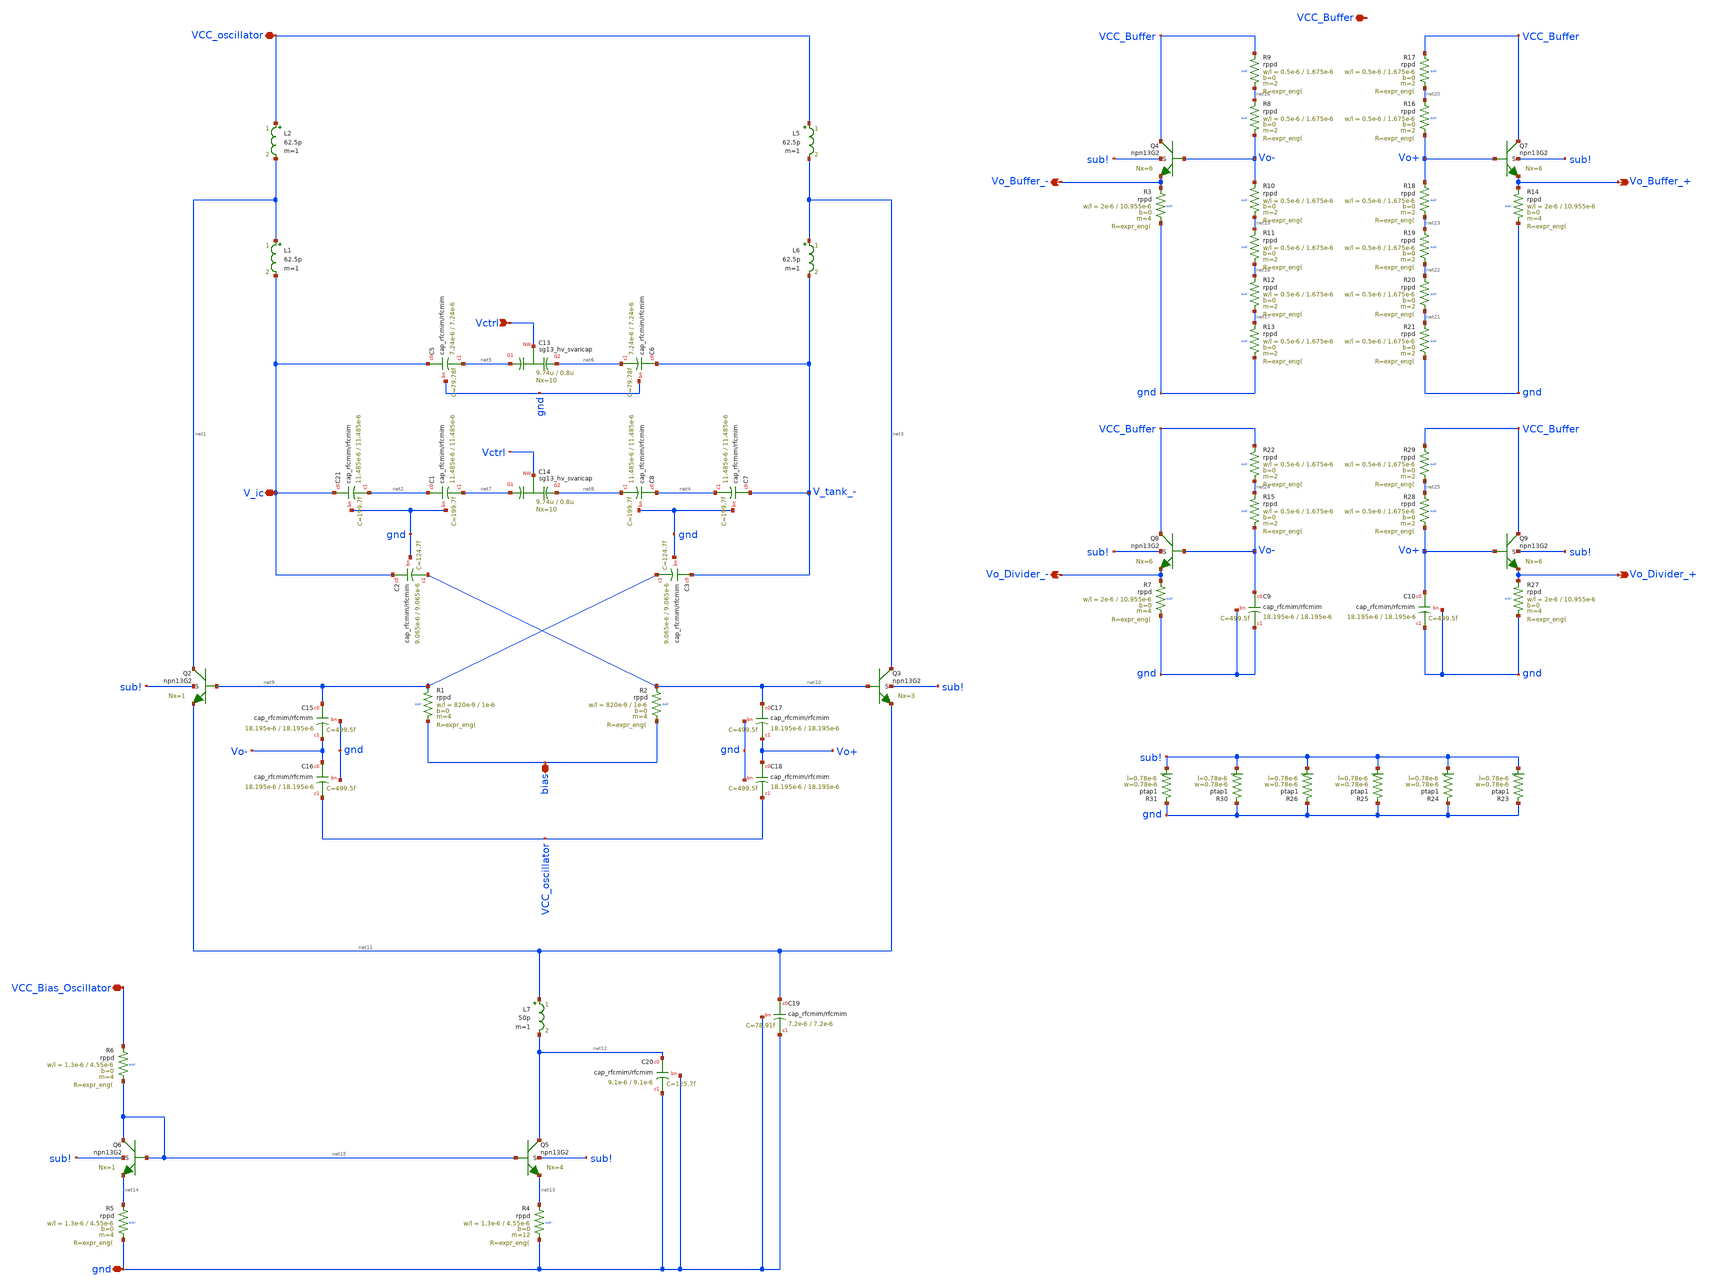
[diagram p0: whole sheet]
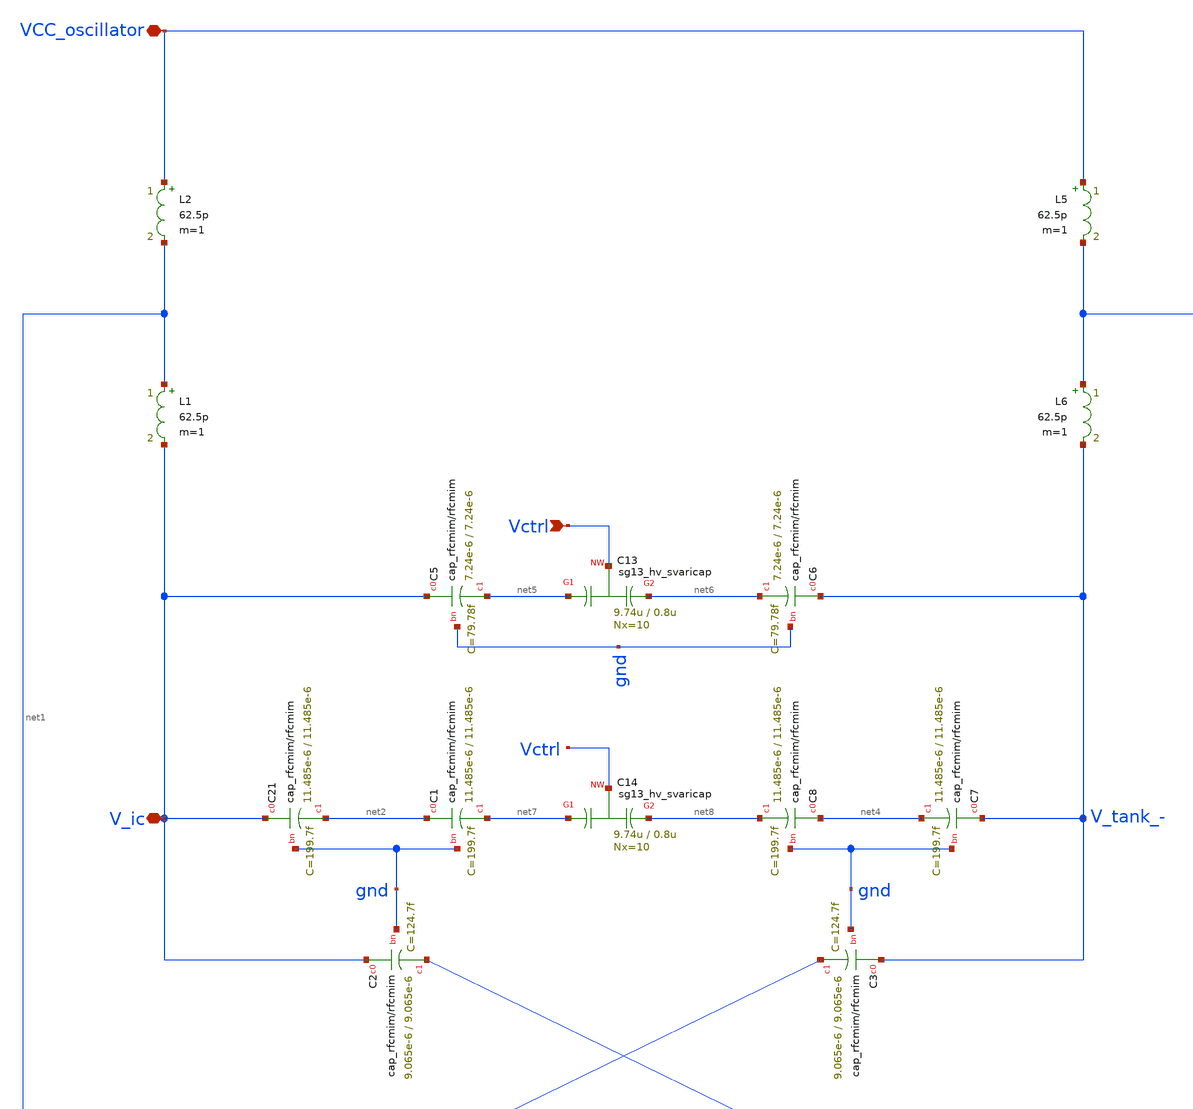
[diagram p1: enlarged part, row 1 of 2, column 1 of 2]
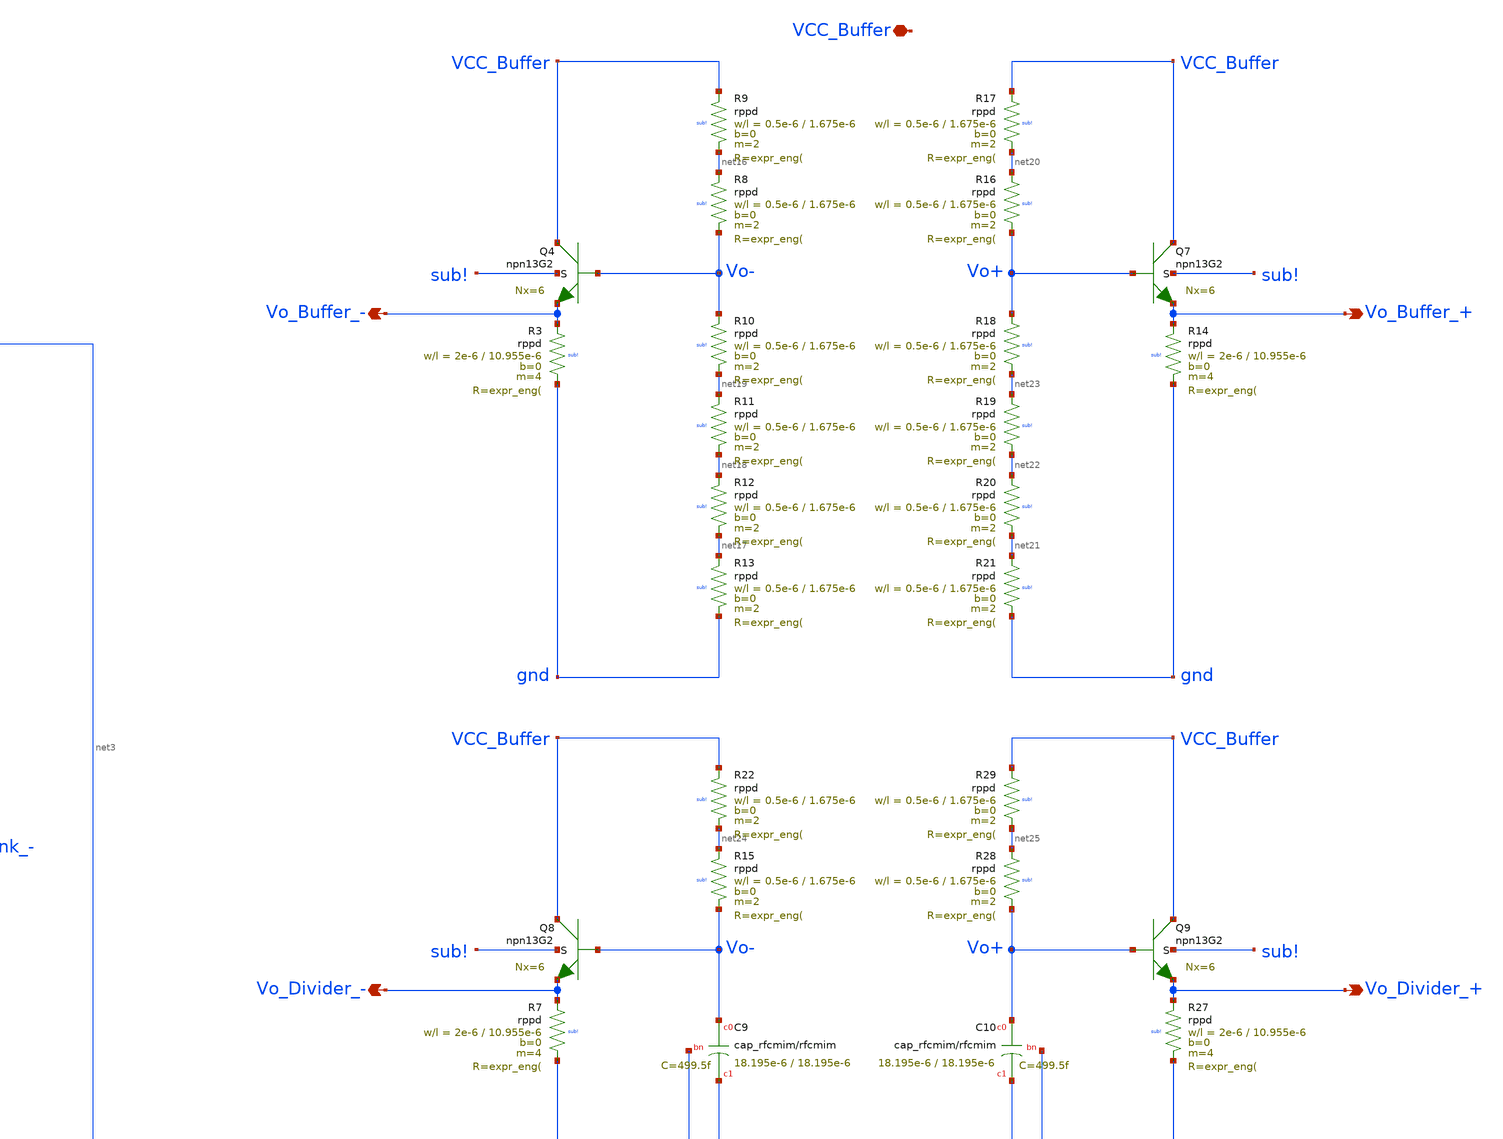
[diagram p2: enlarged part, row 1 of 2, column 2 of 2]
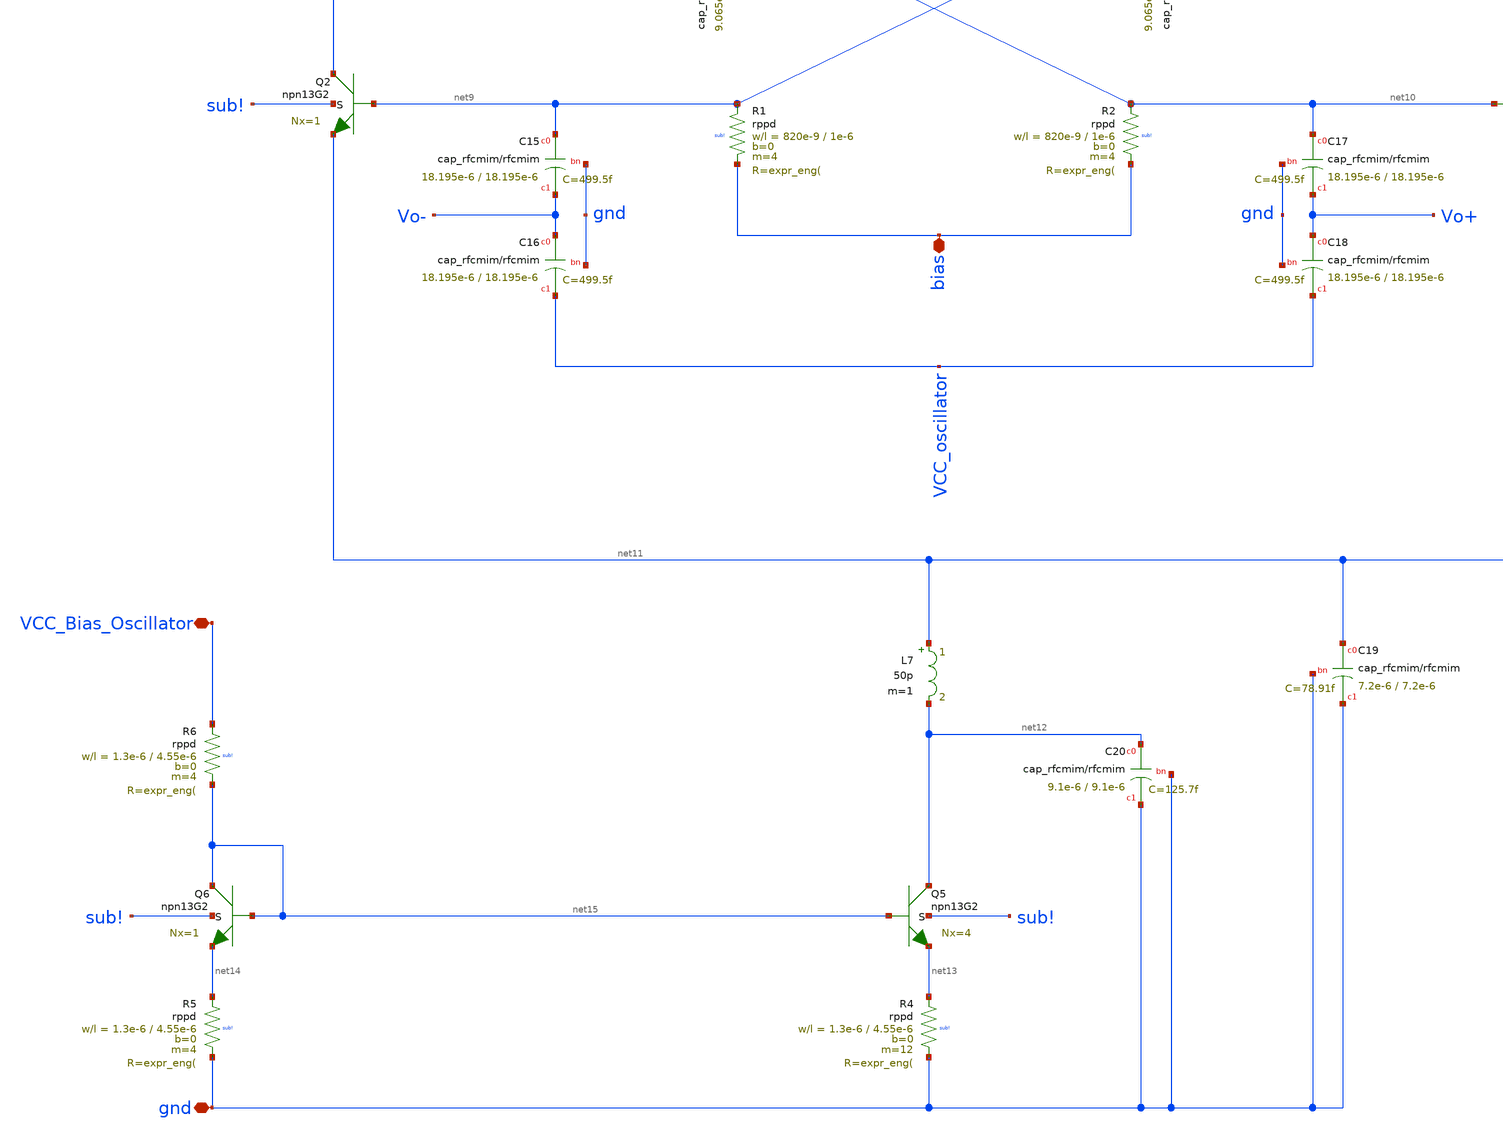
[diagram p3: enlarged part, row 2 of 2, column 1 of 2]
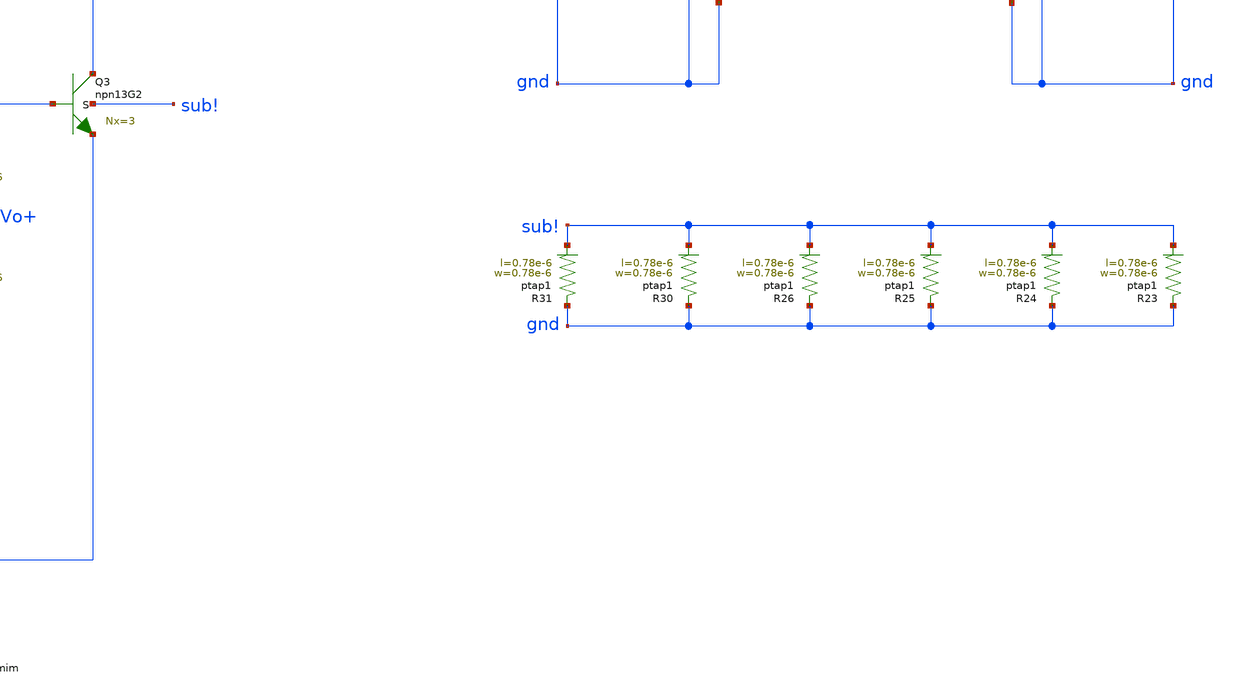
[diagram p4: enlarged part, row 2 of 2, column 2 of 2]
** sch_path: modules/module_4_type_2_PLL/LC_Oscillator/xschem/LC_Oscillator.sch
**.subckt LC_Oscillator VCC_oscillator VCC_Bias_Oscillator Vo_Buffer_- gnd Vctrl VCC_Buffer
*+ Vo_Buffer_+ Vo_Divider_- Vo_Divider_+ bias V_ic
*.iopin VCC_oscillator
*.iopin VCC_Bias_Oscillator
*.opin Vo_Buffer_-
*.iopin gnd
*.ipin Vctrl
*.iopin VCC_Buffer
*.opin Vo_Buffer_+
*.opin Vo_Divider_-
*.opin Vo_Divider_+
*.iopin bias
*.iopin V_ic
XC5 V_ic net5 gnd cap_rfcmim w=7.24e-6 l=7.24e-6 wfeed=5.0e-6 m=1 mm_ok=1
XQ2 net1 net9 net11 sub! npn13G2 Nx=1 mm_ok=1
XC2 V_ic net10 gnd cap_rfcmim w=9.065e-6 l=9.065e-6 wfeed=3.0e-6 m=1 mm_ok=1
XQ3 net3 net10 net11 sub! npn13G2 Nx=3 mm_ok=1
L5 VCC_oscillator net3 62.5p m=1
L6 net3 V_tank_- 62.5p m=1
XC13 net5 Vctrl net6 sub! sg13_hv_svaricap w=9.74u l=0.8u Nx=10 mm_ok=1
XC14 net7 Vctrl net8 sub! sg13_hv_svaricap w=9.74u l=0.8u Nx=10 mm_ok=1
XC15 net9 Vo- gnd cap_rfcmim w=18.195e-6 l=18.195e-6 wfeed=3.0e-6 m=1 mm_ok=1
XC16 Vo- VCC_oscillator gnd cap_rfcmim w=18.195e-6 l=18.195e-6 wfeed=3.0e-6 m=1 mm_ok=1
XR1 net9 bias sub! rppd w=820e-9 l=1e-6 m=4 b=0 mm_ok=1
XC17 net10 Vo+ gnd cap_rfcmim w=18.195e-6 l=18.195e-6 wfeed=3.0e-6 m=1 mm_ok=1
XC18 Vo+ VCC_oscillator gnd cap_rfcmim w=18.195e-6 l=18.195e-6 wfeed=3.0e-6 m=1 mm_ok=1
XR2 net10 bias sub! rppd w=820e-9 l=1e-6 m=4 b=0 mm_ok=1
L7 net11 net12 50p m=1
XC19 net11 gnd gnd cap_rfcmim w=7.2e-6 l=7.2e-6 wfeed=3.0e-6 m=1 mm_ok=1
XQ5 net12 net15 net13 sub! npn13G2 Nx=4 mm_ok=1
XQ6 net15 net15 net14 sub! npn13G2 Nx=1 mm_ok=1
XR4 net13 gnd sub! rppd w=1.3e-6 l=4.55e-6 m=12 b=0 mm_ok=1
XR5 net14 gnd sub! rppd w=1.3e-6 l=4.55e-6 m=4 b=0 mm_ok=1
XR6 VCC_Bias_Oscillator net15 sub! rppd w=1.3e-6 l=4.55e-6 m=4 b=0 mm_ok=1
XC20 net12 gnd gnd cap_rfcmim w=9.1e-6 l=9.1e-6 wfeed=3.0e-6 m=1 mm_ok=1
XC21 V_ic net2 gnd cap_rfcmim w=11.485e-6 l=11.485e-6 wfeed=3.0e-6 m=1 mm_ok=1
XC1 net2 net7 gnd cap_rfcmim w=11.485e-6 l=11.485e-6 wfeed=3.0e-6 m=1 mm_ok=1
XC3 V_tank_- net9 gnd cap_rfcmim w=9.065e-6 l=9.065e-6 wfeed=3.0e-6 m=1 mm_ok=1
XC7 V_tank_- net4 gnd cap_rfcmim w=11.485e-6 l=11.485e-6 wfeed=3.0e-6 m=1 mm_ok=1
XC8 net4 net8 gnd cap_rfcmim w=11.485e-6 l=11.485e-6 wfeed=3.0e-6 m=1 mm_ok=1
XC6 V_tank_- net6 gnd cap_rfcmim w=7.24e-6 l=7.24e-6 wfeed=5.0e-6 m=1 mm_ok=1
L1 net1 V_ic 62.5p m=1
L2 VCC_oscillator net1 62.5p m=1
XQ4 VCC_Buffer Vo- Vo_Buffer_- sub! npn13G2 Nx=6 mm_ok=1
XR3 Vo_Buffer_- gnd sub! rppd w=2e-6 l=10.955e-6 m=4 b=0 mm_ok=1
XR8 net16 Vo- sub! rppd w=0.5e-6 l=1.675e-6 m=2 b=0 mm_ok=1
XR9 VCC_Buffer net16 sub! rppd w=0.5e-6 l=1.675e-6 m=2 b=0 mm_ok=1
XR10 Vo- net19 sub! rppd w=0.5e-6 l=1.675e-6 m=2 b=0 mm_ok=1
XR11 net19 net18 sub! rppd w=0.5e-6 l=1.675e-6 m=2 b=0 mm_ok=1
XR12 net18 net17 sub! rppd w=0.5e-6 l=1.675e-6 m=2 b=0 mm_ok=1
XR13 net17 gnd sub! rppd w=0.5e-6 l=1.675e-6 m=2 b=0 mm_ok=1
XQ7 VCC_Buffer Vo+ Vo_Buffer_+ sub! npn13G2 Nx=6 mm_ok=1
XR14 Vo_Buffer_+ gnd sub! rppd w=2e-6 l=10.955e-6 m=4 b=0 mm_ok=1
XR16 net20 Vo+ sub! rppd w=0.5e-6 l=1.675e-6 m=2 b=0 mm_ok=1
XR17 VCC_Buffer net20 sub! rppd w=0.5e-6 l=1.675e-6 m=2 b=0 mm_ok=1
XR18 Vo+ net23 sub! rppd w=0.5e-6 l=1.675e-6 m=2 b=0 mm_ok=1
XR19 net23 net22 sub! rppd w=0.5e-6 l=1.675e-6 m=2 b=0 mm_ok=1
XR20 net22 net21 sub! rppd w=0.5e-6 l=1.675e-6 m=2 b=0 mm_ok=1
XR21 net21 gnd sub! rppd w=0.5e-6 l=1.675e-6 m=2 b=0 mm_ok=1
XQ8 VCC_Buffer Vo- Vo_Divider_- sub! npn13G2 Nx=6 mm_ok=1
XR7 Vo_Divider_- gnd sub! rppd w=2e-6 l=10.955e-6 m=4 b=0 mm_ok=1
XR15 net24 Vo- sub! rppd w=0.5e-6 l=1.675e-6 m=2 b=0 mm_ok=1
XR22 VCC_Buffer net24 sub! rppd w=0.5e-6 l=1.675e-6 m=2 b=0 mm_ok=1
XQ9 VCC_Buffer Vo+ Vo_Divider_+ sub! npn13G2 Nx=6 mm_ok=1
XR27 Vo_Divider_+ gnd sub! rppd w=2e-6 l=10.955e-6 m=4 b=0 mm_ok=1
XR28 net25 Vo+ sub! rppd w=0.5e-6 l=1.675e-6 m=2 b=0 mm_ok=1
XR29 VCC_Buffer net25 sub! rppd w=0.5e-6 l=1.675e-6 m=2 b=0 mm_ok=1
XC9 Vo- gnd gnd cap_rfcmim w=18.195e-6 l=18.195e-6 wfeed=3.0e-6 m=1 mm_ok=1
XC10 Vo+ gnd gnd cap_rfcmim w=18.195e-6 l=18.195e-6 wfeed=3.0e-6 m=1 mm_ok=1
XR23 gnd sub! ptap1 R=262.8 w=0.78e-6 l=0.78e-6
XR24 gnd sub! ptap1 R=262.8 w=0.78e-6 l=0.78e-6
XR25 gnd sub! ptap1 R=262.8 w=0.78e-6 l=0.78e-6
XR26 gnd sub! ptap1 R=262.8 w=0.78e-6 l=0.78e-6
XR30 gnd sub! ptap1 R=262.8 w=0.78e-6 l=0.78e-6
XR31 gnd sub! ptap1 R=262.8 w=0.78e-6 l=0.78e-6
**.ends
.end
